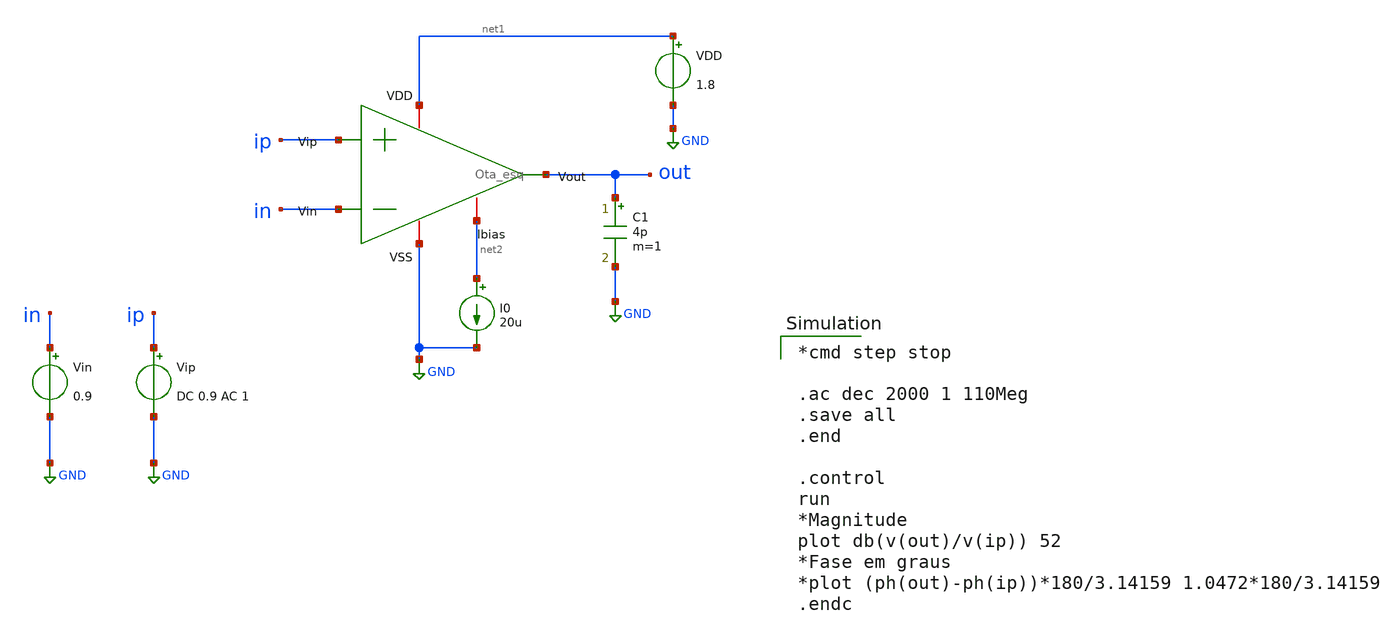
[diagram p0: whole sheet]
** sch_path: xschem/Ota_ac_tb.sch
**.subckt Ota_ac_tb
x1 net1 in ip out net2 GND Ota_esq
Vip ip GND DC 0.9 AC 1
VDD net1 GND 1.8
I0 net2 GND 20u
Vin in GND 0.9
C1 out GND 4p m=1
**** begin user architecture code

** opencircuitdesign pdks install
.lib $::SKYWATER_MODELS/sky130.lib.spice tt



*cmd step stop

.ac dec 2000 1 110Meg
.save all
.end

.control
run
*Magnitude
plot db(v(out)/v(ip)) 52
*Fase em graus
*plot (ph(out)-ph(ip))*180/3.14159 1.0472*180/3.14159
.endc

**** end user architecture code
**.ends

* expanding   symbol:  Ota_esq.sym # of pins=6
** sym_path: Ota_esq.sym
** sch_path: Ota_esq.sch
.subckt Ota_esq VDD Vin Vip Vout Ibias VSS
*.ipin Vin
*.ipin Vip
*.iopin VDD
*.iopin VSS
*.iopin Ibias
*.opin Vout
XM1 net1 Vin net3 net3 sky130_fd_pr__pfet_01v8 L=0.25 W=2.899 nf=1 ad='int((nf+1)/2) * W/nf * 0.29' as='int((nf+2)/2) * W/nf * 0.29'
+ pd='2*int((nf+1)/2) * (W/nf + 0.29)' ps='2*int((nf+2)/2) * (W/nf + 0.29)' nrd='0.29 / W' nrs='0.29 / W'
+ sa=0 sb=0 sd=0 mult=1 m=1
XM2 net2 Vip net3 net3 sky130_fd_pr__pfet_01v8 L=0.25 W=2.899 nf=1 ad='int((nf+1)/2) * W/nf * 0.29' as='int((nf+2)/2) * W/nf * 0.29'
+ pd='2*int((nf+1)/2) * (W/nf + 0.29)' ps='2*int((nf+2)/2) * (W/nf + 0.29)' nrd='0.29 / W' nrs='0.29 / W'
+ sa=0 sb=0 sd=0 mult=1 m=1
XM3 net1 net1 VSS VSS sky130_fd_pr__nfet_01v8 L=0.25 W=0.667 nf=1 ad='int((nf+1)/2) * W/nf * 0.29' as='int((nf+2)/2) * W/nf * 0.29'
+ pd='2*int((nf+1)/2) * (W/nf + 0.29)' ps='2*int((nf+2)/2) * (W/nf + 0.29)' nrd='0.29 / W' nrs='0.29 / W'
+ sa=0 sb=0 sd=0 mult=1 m=1
XM4 net2 net1 VSS VSS sky130_fd_pr__nfet_01v8 L=0.25 W=0.667 nf=1 ad='int((nf+1)/2) * W/nf * 0.29' as='int((nf+2)/2) * W/nf * 0.29'
+ pd='2*int((nf+1)/2) * (W/nf + 0.29)' ps='2*int((nf+2)/2) * (W/nf + 0.29)' nrd='0.29 / W' nrs='0.29 / W'
+ sa=0 sb=0 sd=0 mult=1 m=1
XM5 net3 Ibias VDD VDD sky130_fd_pr__pfet_01v8 L=0.25 W=3.333 nf=1 ad='int((nf+1)/2) * W/nf * 0.29' as='int((nf+2)/2) * W/nf * 0.29'
+ pd='2*int((nf+1)/2) * (W/nf + 0.29)' ps='2*int((nf+2)/2) * (W/nf + 0.29)' nrd='0.29 / W' nrs='0.29 / W'
+ sa=0 sb=0 sd=0 mult=1 m=1
XM8 Ibias Ibias VDD VDD sky130_fd_pr__pfet_01v8 L=0.25 W=3.333 nf=1 ad='int((nf+1)/2) * W/nf * 0.29'
+ as='int((nf+2)/2) * W/nf * 0.29' pd='2*int((nf+1)/2) * (W/nf + 0.29)' ps='2*int((nf+2)/2) * (W/nf + 0.29)'
+ nrd='0.29 / W' nrs='0.29 / W' sa=0 sb=0 sd=0 mult=1 m=1
XM6 Vout Ibias VDD VDD sky130_fd_pr__pfet_01v8 L=0.25 W=17.279 nf=1 ad='int((nf+1)/2) * W/nf * 0.29'
+ as='int((nf+2)/2) * W/nf * 0.29' pd='2*int((nf+1)/2) * (W/nf + 0.29)' ps='2*int((nf+2)/2) * (W/nf + 0.29)'
+ nrd='0.29 / W' nrs='0.29 / W' sa=0 sb=0 sd=0 mult=1 m=1
XM7 Vout net2 VSS VSS sky130_fd_pr__nfet_01v8 L=0.25 W=6.192 nf=1 ad='int((nf+1)/2) * W/nf * 0.29' as='int((nf+2)/2) * W/nf * 0.29'
+ pd='2*int((nf+1)/2) * (W/nf + 0.29)' ps='2*int((nf+2)/2) * (W/nf + 0.29)' nrd='0.29 / W' nrs='0.29 / W'
+ sa=0 sb=0 sd=0 mult=1 m=1
XC1 net2 Vout sky130_fd_pr__cap_mim_m3_1 W=23 L=23 MF=1 m=1
.ends

.GLOBAL GND
.end
